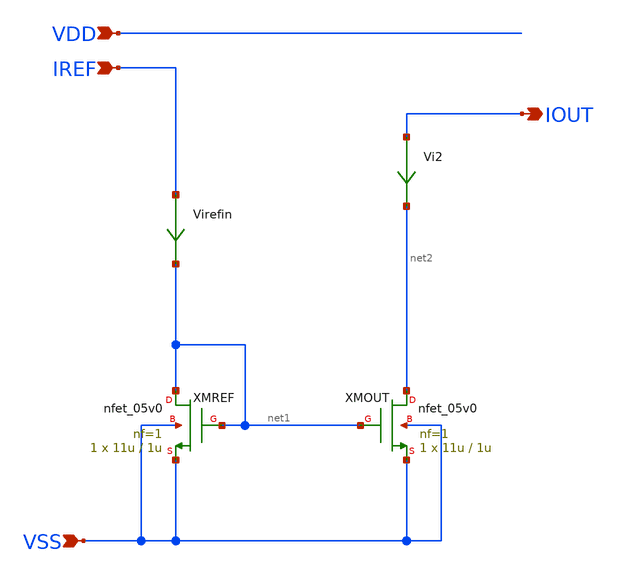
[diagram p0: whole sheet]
** sch_path: blocks/composite/regulated_cascoded_cmirror/Designs/design/cs-vanilla-cm.sch
**.subckt cs-vanilla-cm VDD VSS IREF IOUT
*.ipin VDD
*.ipin VSS
*.ipin IREF
*.opin IOUT
Virefin IREF net1 0
.save i(virefin)
XMREF net1 net1 VSS VSS nfet_05v0 L=1u W=11u nf=1 ad='int((nf+1)/2) * W/nf * 0.18u' as='int((nf+2)/2) * W/nf * 0.18u'
+ pd='2*int((nf+1)/2) * (W/nf + 0.18u)' ps='2*int((nf+2)/2) * (W/nf + 0.18u)' nrd='0.18u / W' nrs='0.18u / W'
+ sa=0 sb=0 sd=0 m=1
XMOUT net2 net1 VSS VSS nfet_05v0 L=1u W=11u nf=1 ad='int((nf+1)/2) * W/nf * 0.18u' as='int((nf+2)/2) * W/nf * 0.18u'
+ pd='2*int((nf+1)/2) * (W/nf + 0.18u)' ps='2*int((nf+2)/2) * (W/nf + 0.18u)' nrd='0.18u / W' nrs='0.18u / W'
+ sa=0 sb=0 sd=0 m=1
Vi2 IOUT net2 0
.save i(vi2)
**.ends
.end
